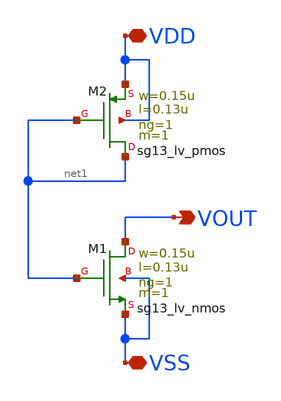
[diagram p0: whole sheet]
** sch_path: CDR4176-main/schematic/xschem/tiel_custom/tiel_custom.sch
**.subckt tiel_custom VDD VSS VOUT
*.iopin VDD
*.iopin VSS
*.opin VOUT
XM2 net1 net1 VDD VDD sg13_lv_pmos w=0.15u l=0.13u ng=1 m=1 mm_ok=1
XM1 VOUT net1 VSS VSS sg13_lv_nmos w=0.15u l=0.13u ng=1 m=1 mm_ok=1
**.ends
.end
